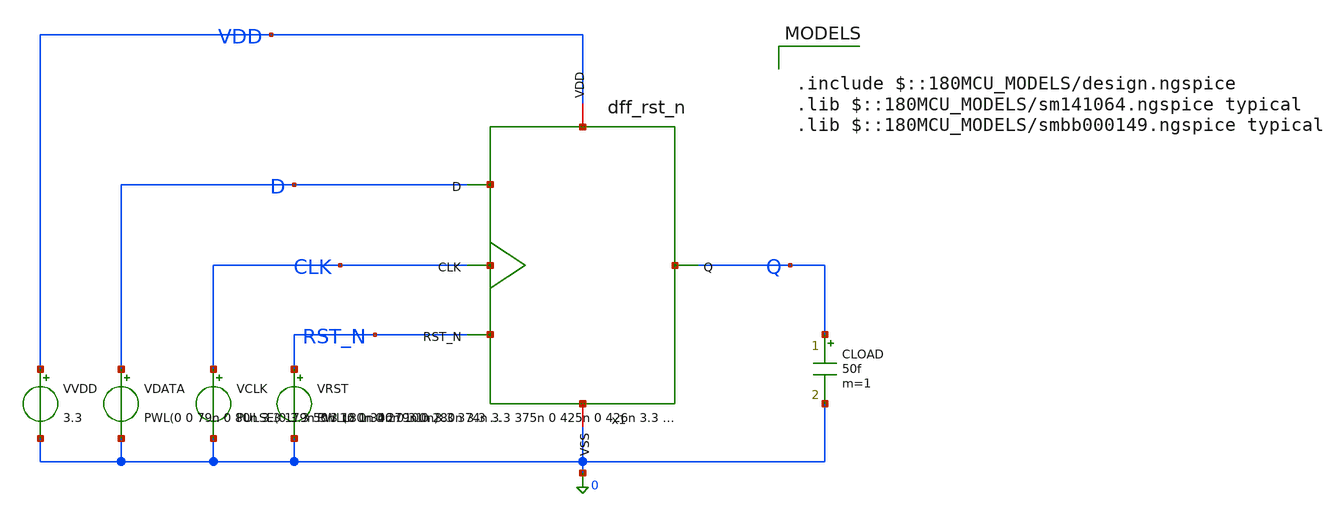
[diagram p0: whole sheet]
** sch_path: sar_logic/sar_designs/dff_rst_n/tb_dff_rst_n.sch
**.subckt tb_dff_rst_n
x1 VDD CLK D Q RST_N 0 dff_rst_n
VRST RST_N 0 PWL(0 0 30n 0 31n 3.3 374n 3.3 375n 0 425n 0 426n 3.3 750n 3.3)
VCLK CLK 0 PULSE(0 3.3 50n 1n 1n 40n 100n)
VDATA D 0 PWL(0 0 79n 0 80n 3.3 179n 3.3 180n 0 279n 0 280n 3.3 399n 3.3 400n 0 479n 0 480n 3.3 579n
+ 3.3 580n 0 750n 0)
VVDD VDD 0 3.3
CLOAD Q 0 50f m=1
**** begin user architecture code

.include $::180MCU_MODELS/design.ngspice
.lib $::180MCU_MODELS/sm141064.ngspice typical
.lib $::180MCU_MODELS/smbb000149.ngspice typical



.options method=gear reltol=1e-3 abstol=1e-12 vntol=1e-6

.control
  save all
  tran 10p 750n

  meas tran q020 FIND v(Q) AT=20n
  meas tran q070 FIND v(Q) AT=70n
  meas tran q120 FIND v(Q) AT=120n
  meas tran q170 FIND v(Q) AT=170n
  meas tran q220 FIND v(Q) AT=220n
  meas tran q270 FIND v(Q) AT=270n
  meas tran q370 FIND v(Q) AT=370n
  meas tran q385 FIND v(Q) AT=385n
  meas tran q415 FIND v(Q) AT=415n
  meas tran q440 FIND v(Q) AT=440n
  meas tran q470 FIND v(Q) AT=470n
  meas tran q570 FIND v(Q) AT=570n
  meas tran q670 FIND v(Q) AT=670n

  meas tran tcq_rise TRIG v(CLK) VAL=1.65 RISE=1 TD=100n TARG v(Q) VAL=1.65 RISE=1 TD=150n
  meas tran tcq_fall TRIG v(CLK) VAL=1.65 RISE=1 TD=200n TARG v(Q) VAL=1.65 FALL=1 TD=250n
  meas tran t_async_rst TRIG v(RST_N) VAL=1.65 FALL=1 TD=300n TARG v(Q) VAL=1.65 FALL=1 TD=374n

  let failures = 0

  if q020 > 0.33
    echo FAIL_q020_reset_did_not_force_Q_low
    let failures = failures + 1
  end

  if q070 > 0.33
    echo FAIL_q070_Q_should_be_low_after_first_edge
    let failures = failures + 1
  end

  if q120 > 0.33
    echo FAIL_q120_Q_changed_before_rising_edge
    let failures = failures + 1
  end

  if q170 < 2.97
    echo FAIL_q170_Q_did_not_capture_high
    let failures = failures + 1
  end

  if q220 < 2.97
    echo FAIL_q220_Q_did_not_hold_high
    let failures = failures + 1
  end

  if q270 > 0.33
    echo FAIL_q270_Q_did_not_capture_low
    let failures = failures + 1
  end

  if q370 < 2.97
    echo FAIL_q370_Q_did_not_capture_high
    let failures = failures + 1
  end

  if q385 > 0.33
    echo FAIL_q385_async_reset_did_not_force_Q_low
    let failures = failures + 1
  end

  if q415 > 0.33
    echo FAIL_q415_Q_did_not_remain_reset
    let failures = failures + 1
  end

  if q440 > 0.33
    echo FAIL_q440_Q_changed_when_reset_was_released
    let failures = failures + 1
  end

  if q470 > 0.33
    echo FAIL_q470_Q_should_capture_low
    let failures = failures + 1
  end

  if q570 < 2.97
    echo FAIL_q570_Q_should_capture_high
    let failures = failures + 1
  end

  if q670 > 0.33
    echo FAIL_q670_Q_should_capture_low
    let failures = failures + 1
  end

  echo
  echo MEASURED_DELAYS
  print tcq_rise tcq_fall t_async_rst
  echo

  if failures < 0.5
    echo PASS_tb_dff_rst_n_all_functional_checks_passed
  else
    echo FAIL_tb_dff_rst_n
    print failures
  end

  write tb_dff_rst_n.raw
  plot v(CLK) v(D) v(RST_N) v(Q)
.endc


**** end user architecture code
**.ends

* expanding   symbol:  dff_rst_n.sym # of pins=6
** sym_path: sar_logic/sar_designs/dff_rst_n.sym
** sch_path: sar_logic/sar_designs/dff_rst_n.sch
.subckt dff_rst_n VDD CLK D Q RST_N VSS
*.ipin D
*.ipin CLK
*.ipin RST_N
*.opin Q
*.iopin VDD
*.iopin VSS
x1 CLK VSS net4 net1 VDD net7 tg
x2 net7 VSS D net1 VDD CLK tg
x3 CLK VSS net4 net2 VDD net7 tg
x4 net7 VSS net6 net2 VDD CLK tg
x5 VDD net3 net1 RST_N VSS nand2
x6 VDD net5 net2 RST_N VSS nand2
x7 VDD net3 net4 VSS inv
x8 VDD net5 Q VSS inv
x9 VDD net5 net6 VSS inv
x10 VDD CLK net7 VSS inv
.ends


* expanding   symbol:  tg.sym # of pins=6
** sym_path: sar_logic/sar_designs/tg.sym
** sch_path: sar_logic/sar_designs/tg.sch
.subckt tg CTRL VSS A B VDD CTRL_B
*.iopin VDD
*.iopin VSS
*.iopin A
*.iopin B
*.ipin CTRL_B
*.ipin CTRL
XM1 A CTRL_B B VDD pfet_03v3 L=0.28u W=1u nf=1 ad='int((nf+1)/2) * W/nf * 0.18u' as='int((nf+2)/2) * W/nf * 0.18u'
+ pd='2*int((nf+1)/2) * (W/nf + 0.18u)' ps='2*int((nf+2)/2) * (W/nf + 0.18u)' nrd='0.18u / W' nrs='0.18u / W'
+ sa=0 sb=0 sd=0 m=1
XM2 A CTRL B VSS nfet_03v3 L=0.28u W=0.5u nf=1 ad='int((nf+1)/2) * W/nf * 0.18u' as='int((nf+2)/2) * W/nf * 0.18u'
+ pd='2*int((nf+1)/2) * (W/nf + 0.18u)' ps='2*int((nf+2)/2) * (W/nf + 0.18u)' nrd='0.18u / W' nrs='0.18u / W'
+ sa=0 sb=0 sd=0 m=1
.ends


* expanding   symbol:  nand2.sym # of pins=5
** sym_path: sar_logic/sar_designs/nand2.sym
** sch_path: sar_logic/sar_designs/nand2.sch
.subckt nand2 VDD Z A B VSS
*.ipin A
*.ipin B
*.iopin VSS
*.iopin VDD
*.opin Z
XM1 Z A VDD VDD pfet_03v3 L=0.28u W=1u nf=1 ad='int((nf+1)/2) * W/nf * 0.18u' as='int((nf+2)/2) * W/nf * 0.18u'
+ pd='2*int((nf+1)/2) * (W/nf + 0.18u)' ps='2*int((nf+2)/2) * (W/nf + 0.18u)' nrd='0.18u / W' nrs='0.18u / W'
+ sa=0 sb=0 sd=0 m=1
XM2 Z B VDD VDD pfet_03v3 L=0.28u W=1u nf=1 ad='int((nf+1)/2) * W/nf * 0.18u' as='int((nf+2)/2) * W/nf * 0.18u'
+ pd='2*int((nf+1)/2) * (W/nf + 0.18u)' ps='2*int((nf+2)/2) * (W/nf + 0.18u)' nrd='0.18u / W' nrs='0.18u / W'
+ sa=0 sb=0 sd=0 m=1
XM3 Z A net1 VSS nfet_03v3 L=0.28u W=1u nf=1 ad='int((nf+1)/2) * W/nf * 0.18u' as='int((nf+2)/2) * W/nf * 0.18u'
+ pd='2*int((nf+1)/2) * (W/nf + 0.18u)' ps='2*int((nf+2)/2) * (W/nf + 0.18u)' nrd='0.18u / W' nrs='0.18u / W'
+ sa=0 sb=0 sd=0 m=1
XM4 net1 B VSS VSS nfet_03v3 L=0.28u W=1u nf=1 ad='int((nf+1)/2) * W/nf * 0.18u' as='int((nf+2)/2) * W/nf * 0.18u'
+ pd='2*int((nf+1)/2) * (W/nf + 0.18u)' ps='2*int((nf+2)/2) * (W/nf + 0.18u)' nrd='0.18u / W' nrs='0.18u / W'
+ sa=0 sb=0 sd=0 m=1
.ends


* expanding   symbol:  inv.sym # of pins=4
** sym_path: sar_logic/sar_designs/inv.sym
** sch_path: sar_logic/sar_designs/inv.sch
.subckt inv VDD vin vout VSS
*.ipin vin
*.opin vout
*.iopin VDD
*.iopin VSS
XM1 vout vin VDD VDD pfet_03v3 L=0.28u W=1u nf=1 ad='int((nf+1)/2) * W/nf * 0.18u' as='int((nf+2)/2) * W/nf * 0.18u'
+ pd='2*int((nf+1)/2) * (W/nf + 0.18u)' ps='2*int((nf+2)/2) * (W/nf + 0.18u)' nrd='0.18u / W' nrs='0.18u / W'
+ sa=0 sb=0 sd=0 m=1
XM2 vout vin VSS VSS nfet_03v3 L=0.28u W=0.5u nf=1 ad='int((nf+1)/2) * W/nf * 0.18u' as='int((nf+2)/2) * W/nf * 0.18u'
+ pd='2*int((nf+1)/2) * (W/nf + 0.18u)' ps='2*int((nf+2)/2) * (W/nf + 0.18u)' nrd='0.18u / W' nrs='0.18u / W'
+ sa=0 sb=0 sd=0 m=1
.ends

.end
